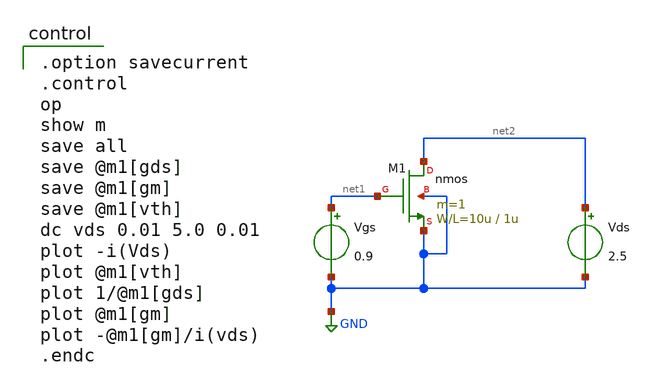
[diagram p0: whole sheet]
** sch_path: OR1/PTC06/opamp/nfet_idvds.sch
**.subckt nfet_idvds
Vgs net1 GND 0.9
Vds net2 GND 2.5
M1 net2 net1 GND GND nmos L=1u W=10u m=1
**** begin user architecture code

.option savecurrent
.control
op
show m
save all
save @m1[gds]
save @m1[gm]
save @m1[vth]
dc vds 0.01 5.0 0.01
plot -i(Vds)
plot @m1[vth]
plot 1/@m1[gds]
plot @m1[gm]
plot -@m1[gm]/i(vds)
.endc

 .include $::LIB/mos.lib
.include $::LIB/passive.lib
.include $::LIB/diode.lib
**** end user architecture code
**.ends
.GLOBAL GND
.end
